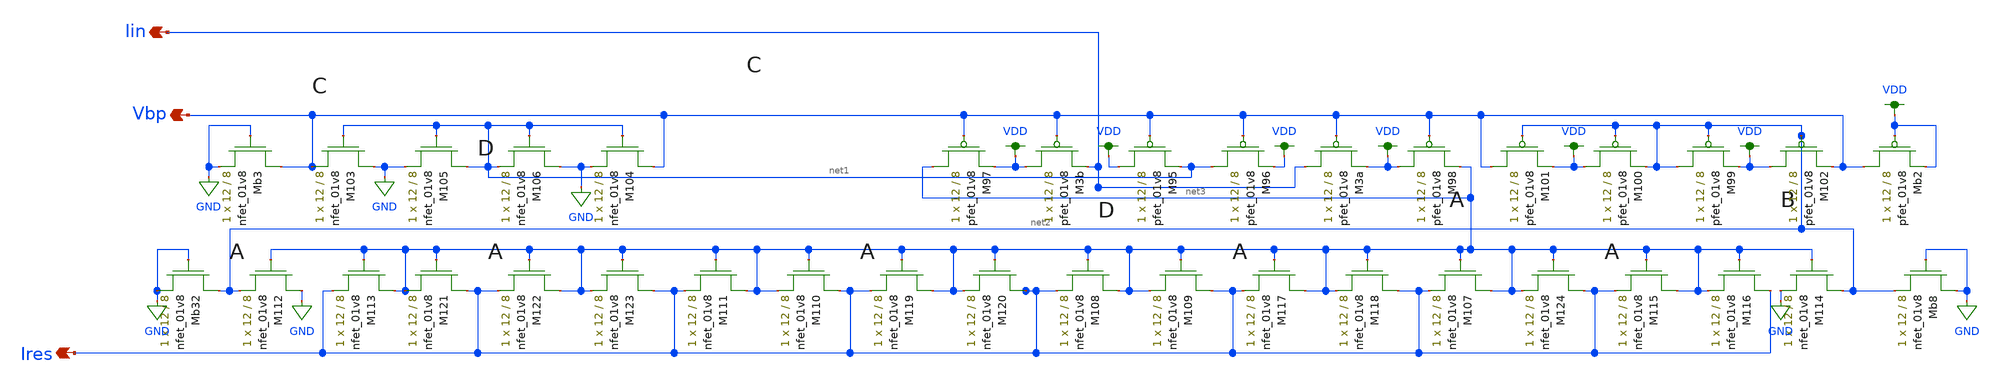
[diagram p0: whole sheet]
** sch_path: final-final-all/xschem/lds/lvs-curgen.sch
**.subckt lvs-curgen Iin Vbp Ires
*.opin Iin
*.opin Vbp
*.opin Ires
XM3b VDD Vbp Iin VDD sky130_fd_pr__pfet_01v8 L=8 W=12 nf=1 ad='int((nf+1)/2) * W/nf * 0.29' as='int((nf+2)/2) * W/nf * 0.29'
+ pd='2*int((nf+1)/2) * (W/nf + 0.29)' ps='2*int((nf+2)/2) * (W/nf + 0.29)' nrd='0.29 / W' nrs='0.29 / W'
+ sa=0 sb=0 sd=0 mult=1 m=1
XM3a Iin Vbp VDD VDD sky130_fd_pr__pfet_01v8 L=8 W=12 nf=1 ad='int((nf+1)/2) * W/nf * 0.29' as='int((nf+2)/2) * W/nf * 0.29'
+ pd='2*int((nf+1)/2) * (W/nf + 0.29)' ps='2*int((nf+2)/2) * (W/nf + 0.29)' nrd='0.29 / W' nrs='0.29 / W'
+ sa=0 sb=0 sd=0 mult=1 m=1
XM95 VDD Vbp net1 VDD sky130_fd_pr__pfet_01v8 L=8 W=12 nf=1 ad='int((nf+1)/2) * W/nf * 0.29' as='int((nf+2)/2) * W/nf * 0.29'
+ pd='2*int((nf+1)/2) * (W/nf + 0.29)' ps='2*int((nf+2)/2) * (W/nf + 0.29)' nrd='0.29 / W' nrs='0.29 / W'
+ sa=0 sb=0 sd=0 mult=1 m=1
XM96 net1 Vbp VDD VDD sky130_fd_pr__pfet_01v8 L=8 W=12 nf=1 ad='int((nf+1)/2) * W/nf * 0.29' as='int((nf+2)/2) * W/nf * 0.29'
+ pd='2*int((nf+1)/2) * (W/nf + 0.29)' ps='2*int((nf+2)/2) * (W/nf + 0.29)' nrd='0.29 / W' nrs='0.29 / W'
+ sa=0 sb=0 sd=0 mult=1 m=1
XM97 net3 Vbp VDD VDD sky130_fd_pr__pfet_01v8 L=8 W=12 nf=1 ad='int((nf+1)/2) * W/nf * 0.29' as='int((nf+2)/2) * W/nf * 0.29'
+ pd='2*int((nf+1)/2) * (W/nf + 0.29)' ps='2*int((nf+2)/2) * (W/nf + 0.29)' nrd='0.29 / W' nrs='0.29 / W'
+ sa=0 sb=0 sd=0 mult=1 m=1
XM98 VDD Vbp net3 VDD sky130_fd_pr__pfet_01v8 L=8 W=12 nf=1 ad='int((nf+1)/2) * W/nf * 0.29' as='int((nf+2)/2) * W/nf * 0.29'
+ pd='2*int((nf+1)/2) * (W/nf + 0.29)' ps='2*int((nf+2)/2) * (W/nf + 0.29)' nrd='0.29 / W' nrs='0.29 / W'
+ sa=0 sb=0 sd=0 mult=1 m=1
XM99 net2 net2 VDD VDD sky130_fd_pr__pfet_01v8 L=8 W=12 nf=1 ad='int((nf+1)/2) * W/nf * 0.29' as='int((nf+2)/2) * W/nf * 0.29'
+ pd='2*int((nf+1)/2) * (W/nf + 0.29)' ps='2*int((nf+2)/2) * (W/nf + 0.29)' nrd='0.29 / W' nrs='0.29 / W'
+ sa=0 sb=0 sd=0 mult=1 m=1
XM100 VDD net2 net2 VDD sky130_fd_pr__pfet_01v8 L=8 W=12 nf=1 ad='int((nf+1)/2) * W/nf * 0.29' as='int((nf+2)/2) * W/nf * 0.29'
+ pd='2*int((nf+1)/2) * (W/nf + 0.29)' ps='2*int((nf+2)/2) * (W/nf + 0.29)' nrd='0.29 / W' nrs='0.29 / W'
+ sa=0 sb=0 sd=0 mult=1 m=1
XM101 Vbp net2 VDD VDD sky130_fd_pr__pfet_01v8 L=8 W=12 nf=1 ad='int((nf+1)/2) * W/nf * 0.29' as='int((nf+2)/2) * W/nf * 0.29'
+ pd='2*int((nf+1)/2) * (W/nf + 0.29)' ps='2*int((nf+2)/2) * (W/nf + 0.29)' nrd='0.29 / W' nrs='0.29 / W'
+ sa=0 sb=0 sd=0 mult=1 m=1
XM102 VDD net2 Vbp VDD sky130_fd_pr__pfet_01v8 L=8 W=12 nf=1 ad='int((nf+1)/2) * W/nf * 0.29' as='int((nf+2)/2) * W/nf * 0.29'
+ pd='2*int((nf+1)/2) * (W/nf + 0.29)' ps='2*int((nf+2)/2) * (W/nf + 0.29)' nrd='0.29 / W' nrs='0.29 / W'
+ sa=0 sb=0 sd=0 mult=1 m=1
XMb2 Vbp VDD VDD VDD sky130_fd_pr__pfet_01v8 L=8 W=12 nf=1 ad='int((nf+1)/2) * W/nf * 0.29' as='int((nf+2)/2) * W/nf * 0.29'
+ pd='2*int((nf+1)/2) * (W/nf + 0.29)' ps='2*int((nf+2)/2) * (W/nf + 0.29)' nrd='0.29 / W' nrs='0.29 / W'
+ sa=0 sb=0 sd=0 mult=1 m=1
XM103 GND net1 Vbp GND sky130_fd_pr__nfet_01v8 L=8 W=12 nf=1 ad='int((nf+1)/2) * W/nf * 0.29' as='int((nf+2)/2) * W/nf * 0.29'
+ pd='2*int((nf+1)/2) * (W/nf + 0.29)' ps='2*int((nf+2)/2) * (W/nf + 0.29)' nrd='0.29 / W' nrs='0.29 / W'
+ sa=0 sb=0 sd=0 mult=1 m=1
XM104 Vbp net1 GND GND sky130_fd_pr__nfet_01v8 L=8 W=12 nf=1 ad='int((nf+1)/2) * W/nf * 0.29' as='int((nf+2)/2) * W/nf * 0.29'
+ pd='2*int((nf+1)/2) * (W/nf + 0.29)' ps='2*int((nf+2)/2) * (W/nf + 0.29)' nrd='0.29 / W' nrs='0.29 / W'
+ sa=0 sb=0 sd=0 mult=1 m=1
XM105 net1 net1 GND GND sky130_fd_pr__nfet_01v8 L=8 W=12 nf=1 ad='int((nf+1)/2) * W/nf * 0.29' as='int((nf+2)/2) * W/nf * 0.29'
+ pd='2*int((nf+1)/2) * (W/nf + 0.29)' ps='2*int((nf+2)/2) * (W/nf + 0.29)' nrd='0.29 / W' nrs='0.29 / W'
+ sa=0 sb=0 sd=0 mult=1 m=1
XM106 GND net1 net1 GND sky130_fd_pr__nfet_01v8 L=8 W=12 nf=1 ad='int((nf+1)/2) * W/nf * 0.29' as='int((nf+2)/2) * W/nf * 0.29'
+ pd='2*int((nf+1)/2) * (W/nf + 0.29)' ps='2*int((nf+2)/2) * (W/nf + 0.29)' nrd='0.29 / W' nrs='0.29 / W'
+ sa=0 sb=0 sd=0 mult=1 m=1
XMb3 Vbp GND GND GND sky130_fd_pr__nfet_01v8 L=8 W=12 nf=1 ad='int((nf+1)/2) * W/nf * 0.29' as='int((nf+2)/2) * W/nf * 0.29'
+ pd='2*int((nf+1)/2) * (W/nf + 0.29)' ps='2*int((nf+2)/2) * (W/nf + 0.29)' nrd='0.29 / W' nrs='0.29 / W'
+ sa=0 sb=0 sd=0 mult=1 m=1
XM107 net3 net3 Ires GND sky130_fd_pr__nfet_01v8 L=8 W=12 nf=1 ad='int((nf+1)/2) * W/nf * 0.29' as='int((nf+2)/2) * W/nf * 0.29'
+ pd='2*int((nf+1)/2) * (W/nf + 0.29)' ps='2*int((nf+2)/2) * (W/nf + 0.29)' nrd='0.29 / W' nrs='0.29 / W'
+ sa=0 sb=0 sd=0 mult=1 m=1
XM108 net3 net3 Ires GND sky130_fd_pr__nfet_01v8 L=8 W=12 nf=1 ad='int((nf+1)/2) * W/nf * 0.29' as='int((nf+2)/2) * W/nf * 0.29'
+ pd='2*int((nf+1)/2) * (W/nf + 0.29)' ps='2*int((nf+2)/2) * (W/nf + 0.29)' nrd='0.29 / W' nrs='0.29 / W'
+ sa=0 sb=0 sd=0 mult=1 m=1
XM109 Ires net3 net3 GND sky130_fd_pr__nfet_01v8 L=8 W=12 nf=1 ad='int((nf+1)/2) * W/nf * 0.29' as='int((nf+2)/2) * W/nf * 0.29'
+ pd='2*int((nf+1)/2) * (W/nf + 0.29)' ps='2*int((nf+2)/2) * (W/nf + 0.29)' nrd='0.29 / W' nrs='0.29 / W'
+ sa=0 sb=0 sd=0 mult=1 m=1
XM110 Ires net3 net3 GND sky130_fd_pr__nfet_01v8 L=8 W=12 nf=1 ad='int((nf+1)/2) * W/nf * 0.29' as='int((nf+2)/2) * W/nf * 0.29'
+ pd='2*int((nf+1)/2) * (W/nf + 0.29)' ps='2*int((nf+2)/2) * (W/nf + 0.29)' nrd='0.29 / W' nrs='0.29 / W'
+ sa=0 sb=0 sd=0 mult=1 m=1
XM111 net3 net3 Ires GND sky130_fd_pr__nfet_01v8 L=8 W=12 nf=1 ad='int((nf+1)/2) * W/nf * 0.29' as='int((nf+2)/2) * W/nf * 0.29'
+ pd='2*int((nf+1)/2) * (W/nf + 0.29)' ps='2*int((nf+2)/2) * (W/nf + 0.29)' nrd='0.29 / W' nrs='0.29 / W'
+ sa=0 sb=0 sd=0 mult=1 m=1
XM112 GND net3 net2 GND sky130_fd_pr__nfet_01v8 L=8 W=12 nf=1 ad='int((nf+1)/2) * W/nf * 0.29' as='int((nf+2)/2) * W/nf * 0.29'
+ pd='2*int((nf+1)/2) * (W/nf + 0.29)' ps='2*int((nf+2)/2) * (W/nf + 0.29)' nrd='0.29 / W' nrs='0.29 / W'
+ sa=0 sb=0 sd=0 mult=1 m=1
XM113 net3 net3 Ires GND sky130_fd_pr__nfet_01v8 L=8 W=12 nf=1 ad='int((nf+1)/2) * W/nf * 0.29' as='int((nf+2)/2) * W/nf * 0.29'
+ pd='2*int((nf+1)/2) * (W/nf + 0.29)' ps='2*int((nf+2)/2) * (W/nf + 0.29)' nrd='0.29 / W' nrs='0.29 / W'
+ sa=0 sb=0 sd=0 mult=1 m=1
XMb8 GND GND net2 GND sky130_fd_pr__nfet_01v8 L=8 W=12 nf=1 ad='int((nf+1)/2) * W/nf * 0.29' as='int((nf+2)/2) * W/nf * 0.29'
+ pd='2*int((nf+1)/2) * (W/nf + 0.29)' ps='2*int((nf+2)/2) * (W/nf + 0.29)' nrd='0.29 / W' nrs='0.29 / W'
+ sa=0 sb=0 sd=0 mult=1 m=1
XM114 net2 net3 GND GND sky130_fd_pr__nfet_01v8 L=8 W=12 nf=1 ad='int((nf+1)/2) * W/nf * 0.29' as='int((nf+2)/2) * W/nf * 0.29'
+ pd='2*int((nf+1)/2) * (W/nf + 0.29)' ps='2*int((nf+2)/2) * (W/nf + 0.29)' nrd='0.29 / W' nrs='0.29 / W'
+ sa=0 sb=0 sd=0 mult=1 m=1
XM115 net3 net3 Ires GND sky130_fd_pr__nfet_01v8 L=8 W=12 nf=1 ad='int((nf+1)/2) * W/nf * 0.29' as='int((nf+2)/2) * W/nf * 0.29'
+ pd='2*int((nf+1)/2) * (W/nf + 0.29)' ps='2*int((nf+2)/2) * (W/nf + 0.29)' nrd='0.29 / W' nrs='0.29 / W'
+ sa=0 sb=0 sd=0 mult=1 m=1
XM116 Ires net3 net3 GND sky130_fd_pr__nfet_01v8 L=8 W=12 nf=1 ad='int((nf+1)/2) * W/nf * 0.29' as='int((nf+2)/2) * W/nf * 0.29'
+ pd='2*int((nf+1)/2) * (W/nf + 0.29)' ps='2*int((nf+2)/2) * (W/nf + 0.29)' nrd='0.29 / W' nrs='0.29 / W'
+ sa=0 sb=0 sd=0 mult=1 m=1
XM117 net3 net3 Ires GND sky130_fd_pr__nfet_01v8 L=8 W=12 nf=1 ad='int((nf+1)/2) * W/nf * 0.29' as='int((nf+2)/2) * W/nf * 0.29'
+ pd='2*int((nf+1)/2) * (W/nf + 0.29)' ps='2*int((nf+2)/2) * (W/nf + 0.29)' nrd='0.29 / W' nrs='0.29 / W'
+ sa=0 sb=0 sd=0 mult=1 m=1
XM118 Ires net3 net3 GND sky130_fd_pr__nfet_01v8 L=8 W=12 nf=1 ad='int((nf+1)/2) * W/nf * 0.29' as='int((nf+2)/2) * W/nf * 0.29'
+ pd='2*int((nf+1)/2) * (W/nf + 0.29)' ps='2*int((nf+2)/2) * (W/nf + 0.29)' nrd='0.29 / W' nrs='0.29 / W'
+ sa=0 sb=0 sd=0 mult=1 m=1
XM119 net3 net3 Ires GND sky130_fd_pr__nfet_01v8 L=8 W=12 nf=1 ad='int((nf+1)/2) * W/nf * 0.29' as='int((nf+2)/2) * W/nf * 0.29'
+ pd='2*int((nf+1)/2) * (W/nf + 0.29)' ps='2*int((nf+2)/2) * (W/nf + 0.29)' nrd='0.29 / W' nrs='0.29 / W'
+ sa=0 sb=0 sd=0 mult=1 m=1
XM120 Ires net3 net3 GND sky130_fd_pr__nfet_01v8 L=8 W=12 nf=1 ad='int((nf+1)/2) * W/nf * 0.29' as='int((nf+2)/2) * W/nf * 0.29'
+ pd='2*int((nf+1)/2) * (W/nf + 0.29)' ps='2*int((nf+2)/2) * (W/nf + 0.29)' nrd='0.29 / W' nrs='0.29 / W'
+ sa=0 sb=0 sd=0 mult=1 m=1
XM121 Ires net3 net3 GND sky130_fd_pr__nfet_01v8 L=8 W=12 nf=1 ad='int((nf+1)/2) * W/nf * 0.29' as='int((nf+2)/2) * W/nf * 0.29'
+ pd='2*int((nf+1)/2) * (W/nf + 0.29)' ps='2*int((nf+2)/2) * (W/nf + 0.29)' nrd='0.29 / W' nrs='0.29 / W'
+ sa=0 sb=0 sd=0 mult=1 m=1
XM122 net3 net3 Ires GND sky130_fd_pr__nfet_01v8 L=8 W=12 nf=1 ad='int((nf+1)/2) * W/nf * 0.29' as='int((nf+2)/2) * W/nf * 0.29'
+ pd='2*int((nf+1)/2) * (W/nf + 0.29)' ps='2*int((nf+2)/2) * (W/nf + 0.29)' nrd='0.29 / W' nrs='0.29 / W'
+ sa=0 sb=0 sd=0 mult=1 m=1
XM123 Ires net3 net3 GND sky130_fd_pr__nfet_01v8 L=8 W=12 nf=1 ad='int((nf+1)/2) * W/nf * 0.29' as='int((nf+2)/2) * W/nf * 0.29'
+ pd='2*int((nf+1)/2) * (W/nf + 0.29)' ps='2*int((nf+2)/2) * (W/nf + 0.29)' nrd='0.29 / W' nrs='0.29 / W'
+ sa=0 sb=0 sd=0 mult=1 m=1
XMb32 net2 GND GND GND sky130_fd_pr__nfet_01v8 L=8 W=12 nf=1 ad='int((nf+1)/2) * W/nf * 0.29' as='int((nf+2)/2) * W/nf * 0.29'
+ pd='2*int((nf+1)/2) * (W/nf + 0.29)' ps='2*int((nf+2)/2) * (W/nf + 0.29)' nrd='0.29 / W' nrs='0.29 / W'
+ sa=0 sb=0 sd=0 mult=1 m=1
XM124 Ires net3 net3 GND sky130_fd_pr__nfet_01v8 L=8 W=12 nf=1 ad='int((nf+1)/2) * W/nf * 0.29' as='int((nf+2)/2) * W/nf * 0.29'
+ pd='2*int((nf+1)/2) * (W/nf + 0.29)' ps='2*int((nf+2)/2) * (W/nf + 0.29)' nrd='0.29 / W' nrs='0.29 / W'
+ sa=0 sb=0 sd=0 mult=1 m=1
**.ends
.GLOBAL VDD
.GLOBAL GND
.end
